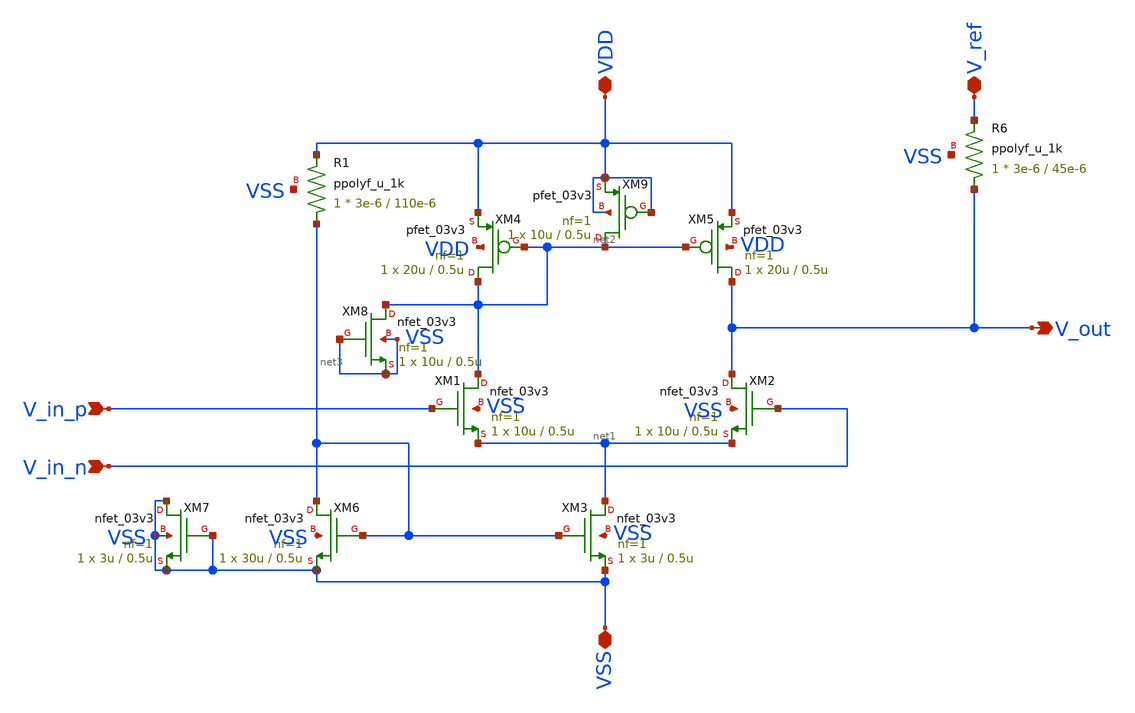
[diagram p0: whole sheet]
** sch_path: schematics/tanh_ota.sch
**.subckt tanh_ota VDD VSS V_in_p V_in_n V_out V_ref
*.iopin VDD
*.iopin VSS
*.ipin V_in_p
*.ipin V_in_n
*.opin V_out
*.iopin V_ref
XM1 net2 V_in_p net1 VSS nfet_03v3 L=0.5u W=10u nf=1 ad='int((nf+1)/2) * W/nf * 0.18u' as='int((nf+2)/2) * W/nf * 0.18u'
+ pd='2*int((nf+1)/2) * (W/nf + 0.18u)' ps='2*int((nf+2)/2) * (W/nf + 0.18u)' nrd='0.18u / W' nrs='0.18u / W'
+ sa=0 sb=0 sd=0 m=1
XM2 V_out V_in_n net1 VSS nfet_03v3 L=0.5u W=10u nf=1 ad='int((nf+1)/2) * W/nf * 0.18u' as='int((nf+2)/2) * W/nf * 0.18u'
+ pd='2*int((nf+1)/2) * (W/nf + 0.18u)' ps='2*int((nf+2)/2) * (W/nf + 0.18u)' nrd='0.18u / W' nrs='0.18u / W'
+ sa=0 sb=0 sd=0 m=1
XM3 net1 net3 VSS VSS nfet_03v3 L=0.5u W=3u nf=1 ad='int((nf+1)/2) * W/nf * 0.18u' as='int((nf+2)/2) * W/nf * 0.18u'
+ pd='2*int((nf+1)/2) * (W/nf + 0.18u)' ps='2*int((nf+2)/2) * (W/nf + 0.18u)' nrd='0.18u / W' nrs='0.18u / W'
+ sa=0 sb=0 sd=0 m=1
XM4 net2 net2 VDD VDD pfet_03v3 L=0.5u W=20u nf=1 ad='int((nf+1)/2) * W/nf * 0.18u' as='int((nf+2)/2) * W/nf * 0.18u'
+ pd='2*int((nf+1)/2) * (W/nf + 0.18u)' ps='2*int((nf+2)/2) * (W/nf + 0.18u)' nrd='0.18u / W' nrs='0.18u / W'
+ sa=0 sb=0 sd=0 m=1
XM5 V_out net2 VDD VDD pfet_03v3 L=0.5u W=20u nf=1 ad='int((nf+1)/2) * W/nf * 0.18u' as='int((nf+2)/2) * W/nf * 0.18u'
+ pd='2*int((nf+1)/2) * (W/nf + 0.18u)' ps='2*int((nf+2)/2) * (W/nf + 0.18u)' nrd='0.18u / W' nrs='0.18u / W'
+ sa=0 sb=0 sd=0 m=1
XR6 V_out V_ref VSS ppolyf_u_1k r_width=3e-6 r_length=45e-6 m=1
XM6 net3 net3 VSS VSS nfet_03v3 L=0.5u W=30u nf=1 ad='int((nf+1)/2) * W/nf * 0.18u' as='int((nf+2)/2) * W/nf * 0.18u'
+ pd='2*int((nf+1)/2) * (W/nf + 0.18u)' ps='2*int((nf+2)/2) * (W/nf + 0.18u)' nrd='0.18u / W' nrs='0.18u / W'
+ sa=0 sb=0 sd=0 m=1
XR1 net3 VDD VSS ppolyf_u_1k r_width=3e-6 r_length=110e-6 m=1
XM7 VSS VSS VSS VSS nfet_03v3 L=0.5u W=3u nf=1 ad='int((nf+1)/2) * W/nf * 0.18u' as='int((nf+2)/2) * W/nf * 0.18u'
+ pd='2*int((nf+1)/2) * (W/nf + 0.18u)' ps='2*int((nf+2)/2) * (W/nf + 0.18u)' nrd='0.18u / W' nrs='0.18u / W'
+ sa=0 sb=0 sd=0 m=1
XM8 net2 VSS VSS VSS nfet_03v3 L=0.5u W=10u nf=1 ad='int((nf+1)/2) * W/nf * 0.18u' as='int((nf+2)/2) * W/nf * 0.18u'
+ pd='2*int((nf+1)/2) * (W/nf + 0.18u)' ps='2*int((nf+2)/2) * (W/nf + 0.18u)' nrd='0.18u / W' nrs='0.18u / W'
+ sa=0 sb=0 sd=0 m=1
XM9 net2 VDD VDD VDD pfet_03v3 L=0.5u W=10u nf=1 ad='int((nf+1)/2) * W/nf * 0.18u' as='int((nf+2)/2) * W/nf * 0.18u'
+ pd='2*int((nf+1)/2) * (W/nf + 0.18u)' ps='2*int((nf+2)/2) * (W/nf + 0.18u)' nrd='0.18u / W' nrs='0.18u / W'
+ sa=0 sb=0 sd=0 m=1
**.ends
.end
